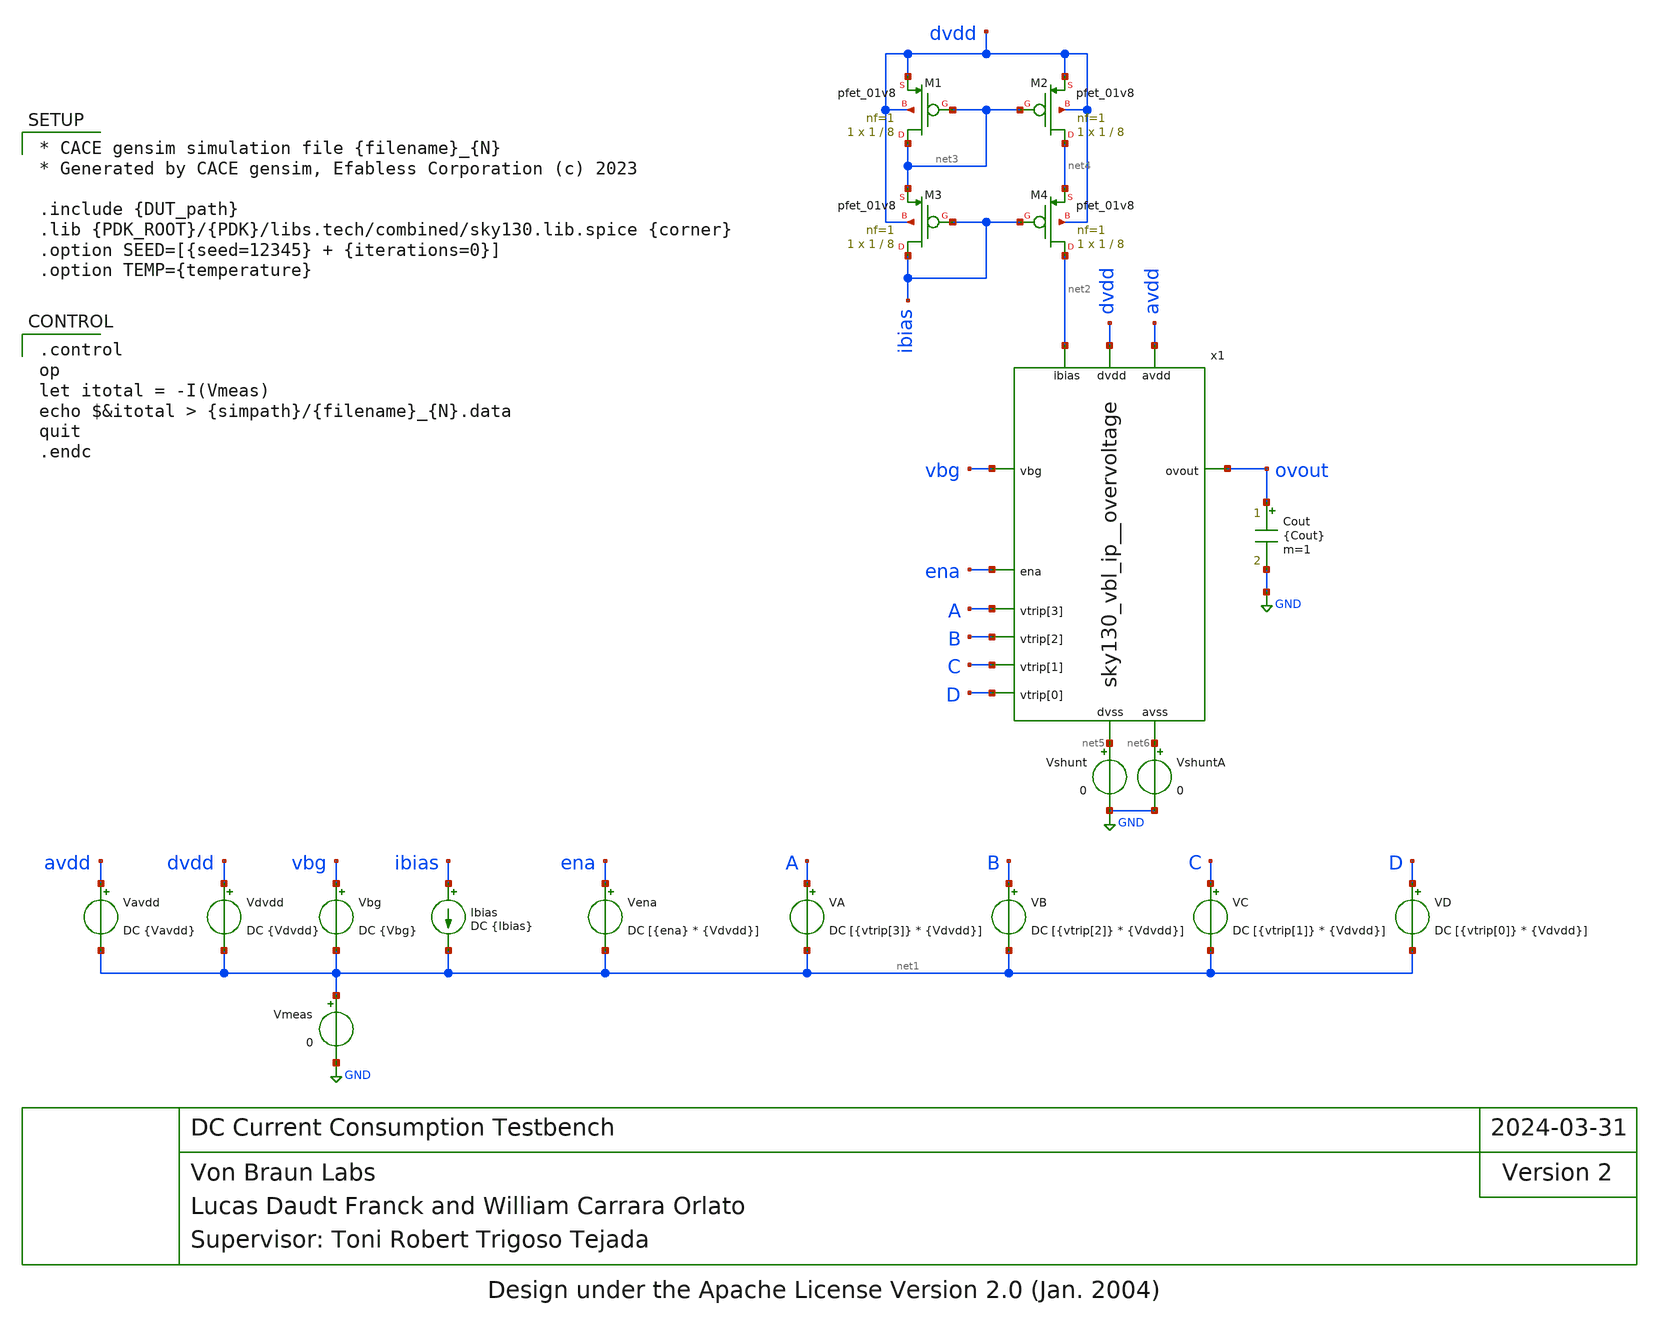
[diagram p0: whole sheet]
** sch_path: cace/tb_dccurrent.sch
* Design under the Apache License Version 2.0 (Jan. 2004)
**.subckt tb_dccurrent
Cout ovout GND {Cout} m=1
Vavdd avdd net1 DC {Vavdd}
Vdvdd dvdd net1 DC {Vdvdd}
Vena ena net1 DC [{ena} * {Vdvdd}]
VA A net1 DC [{vtrip[3]} * {Vdvdd}]
VB B net1 DC [{vtrip[2]} * {Vdvdd}]
VC C net1 DC [{vtrip[1]} * {Vdvdd}]
VD D net1 DC [{vtrip[0]} * {Vdvdd}]
Vbg vbg net1 DC {Vbg}
Ibias ibias net1 DC {Ibias}
Vmeas net1 GND 0
XM1 net3 net3 dvdd dvdd sky130_fd_pr__pfet_01v8 L=8 W=1 nf=1 ad='int((nf+1)/2) * W/nf * 0.29' as='int((nf+2)/2) * W/nf * 0.29'
+ pd='2*int((nf+1)/2) * (W/nf + 0.29)' ps='2*int((nf+2)/2) * (W/nf + 0.29)' nrd='0.29 / W' nrs='0.29 / W'
+ sa=0 sb=0 sd=0 mult=1 m=1
XM2 net4 net3 dvdd dvdd sky130_fd_pr__pfet_01v8 L=8 W=1 nf=1 ad='int((nf+1)/2) * W/nf * 0.29' as='int((nf+2)/2) * W/nf * 0.29'
+ pd='2*int((nf+1)/2) * (W/nf + 0.29)' ps='2*int((nf+2)/2) * (W/nf + 0.29)' nrd='0.29 / W' nrs='0.29 / W'
+ sa=0 sb=0 sd=0 mult=1 m=1
XM3 ibias ibias net3 dvdd sky130_fd_pr__pfet_01v8 L=8 W=1 nf=1 ad='int((nf+1)/2) * W/nf * 0.29' as='int((nf+2)/2) * W/nf * 0.29'
+ pd='2*int((nf+1)/2) * (W/nf + 0.29)' ps='2*int((nf+2)/2) * (W/nf + 0.29)' nrd='0.29 / W' nrs='0.29 / W'
+ sa=0 sb=0 sd=0 mult=1 m=1
XM4 net2 ibias net4 dvdd sky130_fd_pr__pfet_01v8 L=8 W=1 nf=1 ad='int((nf+1)/2) * W/nf * 0.29' as='int((nf+2)/2) * W/nf * 0.29'
+ pd='2*int((nf+1)/2) * (W/nf + 0.29)' ps='2*int((nf+2)/2) * (W/nf + 0.29)' nrd='0.29 / W' nrs='0.29 / W'
+ sa=0 sb=0 sd=0 mult=1 m=1
x1 avdd dvdd ena A net2 B ovout vbg C D net5 net6 sky130_vbl_ip__overvoltage
Vshunt net5 GND 0
VshuntA net6 GND 0
**** begin user architecture code

* CACE gensim simulation file {filename}_{N}
* Generated by CACE gensim, Efabless Corporation (c) 2023

.include {DUT_path}
.lib {PDK_ROOT}/{PDK}/libs.tech/combined/sky130.lib.spice {corner}
.option SEED=[{seed=12345} + {iterations=0}]
.option TEMP={temperature}



.control
op
let itotal = -I(Vmeas)
echo $&itotal > {simpath}/{filename}_{N}.data
quit
.endc


**** end user architecture code
**.ends
.GLOBAL GND
.end
